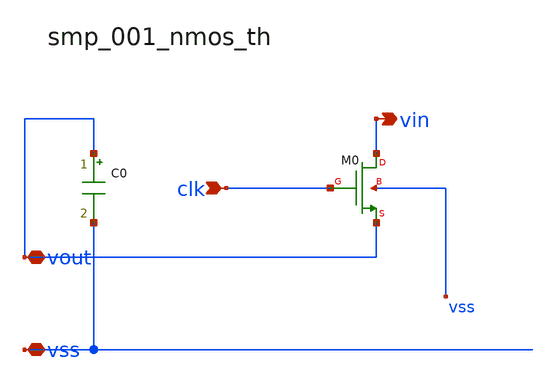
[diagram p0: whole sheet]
** sch_path: analog-db/raw/smp_001_nmos_th/smp_001_nmos_th.sch
**.subckt smp_001_nmos_th clk vout vss vin
*.ipin clk
*.iopin vout
*.iopin vss
*.opin vin
C0 vout vss x_dut_c0_value m=1
XM0 vin clk vout vss sg13_lv_nmos w=x_dut_xm0_w l=x_dut_xm0_l ng=1 m=x_dut_xm0_m
**.ends
.end
